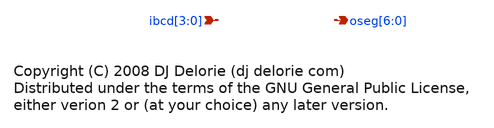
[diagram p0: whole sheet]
** sch_path: xschem_libs_newsym/binto7seg/sevenseg/schematic/sevenseg.sch
* Copyright (C) 1998-2024 Stefan Frederik Schippers
* This program is free software; you can redistribute it and/or modify
* it under the terms of the GNU General Public License as published by
* the Free Software Foundation; either version 2 of the License, or
* (at your option) any later version.
* This program is distributed in the hope that it will be useful,
* but WITHOUT ANY WARRANTY; without even the implied warranty of
* MERCHANTABILITY or FITNESS FOR A PARTICULAR PURPOSE.  See the
* GNU General Public License for more details.
* You should have received a copy of the GNU General Public License
* along with this program; if not, write to the Free Software
**.subckt sevenseg ibcd[3],ibcd[2],ibcd[1],ibcd[0]
*+ oseg[6],oseg[5],oseg[4],oseg[3],oseg[2],oseg[1],oseg[0]
*.ipin ibcd[3],ibcd[2],ibcd[1],ibcd[0]
*.opin oseg[6],oseg[5],oseg[4],oseg[3],oseg[2],oseg[1],oseg[0]
**** begin user architecture code

// Copyright (C) 2008 DJ Delorie <dj delorie com>
// Distributed under the terms of the GNU General Public License,
// either verion 2 or (at your choice) any later version.

always @ (ibcd)
begin
  case (ibcd)  // abcdefg
    0 : oseg = 7'b1111110;
    1 : oseg = 7'b0110000;
    2 : oseg = 7'b1101101;
    3 : oseg = 7'b1111001;
    4 : oseg = 7'b0110011;
    5 : oseg = 7'b1011011;
    6 : oseg = 7'b1011111;
    7 : oseg = 7'b1110000;
    8 : oseg = 7'b1111111;
    9 : oseg = 7'b1111011;
    default : oseg = 0;
  endcase
end



**** end user architecture code
**.ends
.end
